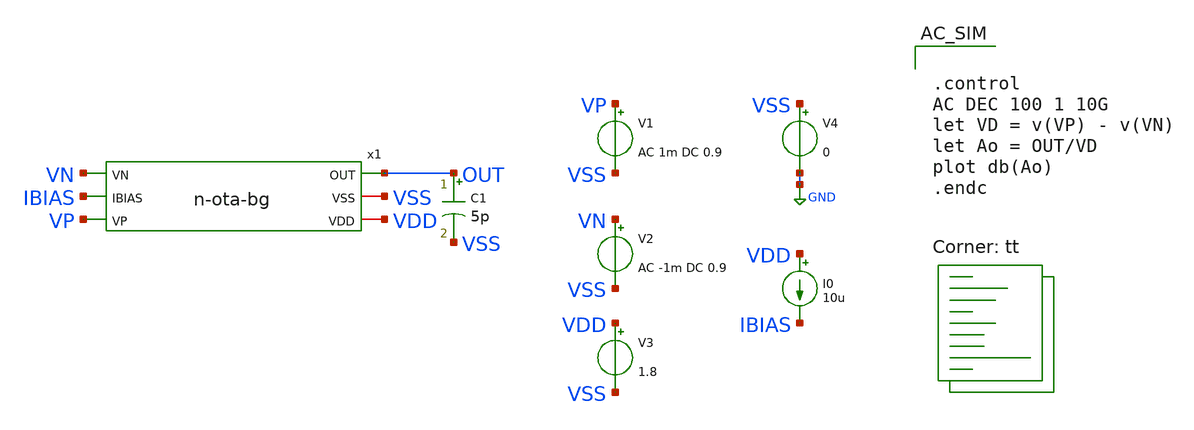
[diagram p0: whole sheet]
** sch_path: designs/libs/core_tb/tb_bg-ota/bgr-ota-ao.sch
**.subckt bgr-ota-ao
V1 VP VSS AC 1m DC 0.9
V2 VN VSS AC -1m DC 0.9
V3 VDD VSS 1.8
V4 VSS GND 0
I0 VDD IBIAS 10u
x1 VN OUT IBIAS VSS VP VDD n-ota-bg
C1 OUT VSS 5p m=1
**** begin user architecture code
.lib $::SKYWATER_MODELS/sky130.lib.spice tt


.control
AC DEC 100 1 10G
let VD = v(VP) - v(VN)
let Ao = OUT/VD
plot db(Ao)
.endc


**** end user architecture code
**.ends

* expanding   symbol:
*+  bandgap-referenced-ota/designs/libs/core_analog/core_bandgap/5t-ota/n-ota-bg.sym # of pins=6
** sym_path: designs/libs/core_analog/core_bandgap/5t-ota/n-ota-bg.sym
** sch_path: designs/libs/core_analog/core_bandgap/5t-ota/n-ota-bg.sch
.subckt n-ota-bg VN OUT IBIAS VSS VP VDD
*.iopin VDD
*.iopin VSS
*.ipin IBIAS
*.ipin VP
*.ipin VN
*.opin OUT
XM1 net2 VP net1 VSS sky130_fd_pr__nfet_01v8 L=4 W=4 nf=1 ad='int((nf+1)/2) * W/nf * 0.29' as='int((nf+2)/2) * W/nf * 0.29'
+ pd='2*int((nf+1)/2) * (W/nf + 0.29)' ps='2*int((nf+2)/2) * (W/nf + 0.29)' nrd='0.29 / W' nrs='0.29 / W'
+ sa=0 sb=0 sd=0 mult=1 m=1
XM2 net3 VN net1 VSS sky130_fd_pr__nfet_01v8 L=4 W=4 nf=1 ad='int((nf+1)/2) * W/nf * 0.29' as='int((nf+2)/2) * W/nf * 0.29'
+ pd='2*int((nf+1)/2) * (W/nf + 0.29)' ps='2*int((nf+2)/2) * (W/nf + 0.29)' nrd='0.29 / W' nrs='0.29 / W'
+ sa=0 sb=0 sd=0 mult=1 m=1
XM3 net1 IBIAS VSS VSS sky130_fd_pr__nfet_01v8 L=4 W=4 nf=1 ad='int((nf+1)/2) * W/nf * 0.29' as='int((nf+2)/2) * W/nf * 0.29'
+ pd='2*int((nf+1)/2) * (W/nf + 0.29)' ps='2*int((nf+2)/2) * (W/nf + 0.29)' nrd='0.29 / W' nrs='0.29 / W'
+ sa=0 sb=0 sd=0 mult=1 m=1
XM4 net3 net2 VDD VDD sky130_fd_pr__pfet_01v8 L=4 W=8 nf=1 ad='int((nf+1)/2) * W/nf * 0.29' as='int((nf+2)/2) * W/nf * 0.29'
+ pd='2*int((nf+1)/2) * (W/nf + 0.29)' ps='2*int((nf+2)/2) * (W/nf + 0.29)' nrd='0.29 / W' nrs='0.29 / W'
+ sa=0 sb=0 sd=0 mult=1 m=1
XM5 net2 net2 VDD VDD sky130_fd_pr__pfet_01v8 L=4 W=8 nf=1 ad='int((nf+1)/2) * W/nf * 0.29' as='int((nf+2)/2) * W/nf * 0.29'
+ pd='2*int((nf+1)/2) * (W/nf + 0.29)' ps='2*int((nf+2)/2) * (W/nf + 0.29)' nrd='0.29 / W' nrs='0.29 / W'
+ sa=0 sb=0 sd=0 mult=1 m=1
XM6 IBIAS IBIAS VSS VSS sky130_fd_pr__nfet_01v8 L=4 W=4 nf=1 ad='int((nf+1)/2) * W/nf * 0.29' as='int((nf+2)/2) * W/nf * 0.29'
+ pd='2*int((nf+1)/2) * (W/nf + 0.29)' ps='2*int((nf+2)/2) * (W/nf + 0.29)' nrd='0.29 / W' nrs='0.29 / W'
+ sa=0 sb=0 sd=0 mult=1 m=1
XM7 net3 net2 VDD VDD sky130_fd_pr__pfet_01v8 L=4 W=8 nf=1 ad='int((nf+1)/2) * W/nf * 0.29' as='int((nf+2)/2) * W/nf * 0.29'
+ pd='2*int((nf+1)/2) * (W/nf + 0.29)' ps='2*int((nf+2)/2) * (W/nf + 0.29)' nrd='0.29 / W' nrs='0.29 / W'
+ sa=0 sb=0 sd=0 mult=1 m=1
XM8 net2 net2 VDD VDD sky130_fd_pr__pfet_01v8 L=4 W=8 nf=1 ad='int((nf+1)/2) * W/nf * 0.29' as='int((nf+2)/2) * W/nf * 0.29'
+ pd='2*int((nf+1)/2) * (W/nf + 0.29)' ps='2*int((nf+2)/2) * (W/nf + 0.29)' nrd='0.29 / W' nrs='0.29 / W'
+ sa=0 sb=0 sd=0 mult=1 m=1
XM9 OUT net3 VDD VDD sky130_fd_pr__pfet_01v8 L=2 W=18 nf=1 ad='int((nf+1)/2) * W/nf * 0.29' as='int((nf+2)/2) * W/nf * 0.29'
+ pd='2*int((nf+1)/2) * (W/nf + 0.29)' ps='2*int((nf+2)/2) * (W/nf + 0.29)' nrd='0.29 / W' nrs='0.29 / W'
+ sa=0 sb=0 sd=0 mult=1 m=1
XM10 OUT IBIAS VSS VSS sky130_fd_pr__nfet_01v8 L=2 W=2 nf=1 ad='int((nf+1)/2) * W/nf * 0.29' as='int((nf+2)/2) * W/nf * 0.29'
+ pd='2*int((nf+1)/2) * (W/nf + 0.29)' ps='2*int((nf+2)/2) * (W/nf + 0.29)' nrd='0.29 / W' nrs='0.29 / W'
+ sa=0 sb=0 sd=0 mult=1 m=1
XC1 OUT net3 sky130_fd_pr__cap_mim_m3_1 W=25 L=1 MF=1 m=1
.ends

.GLOBAL GND
.end
